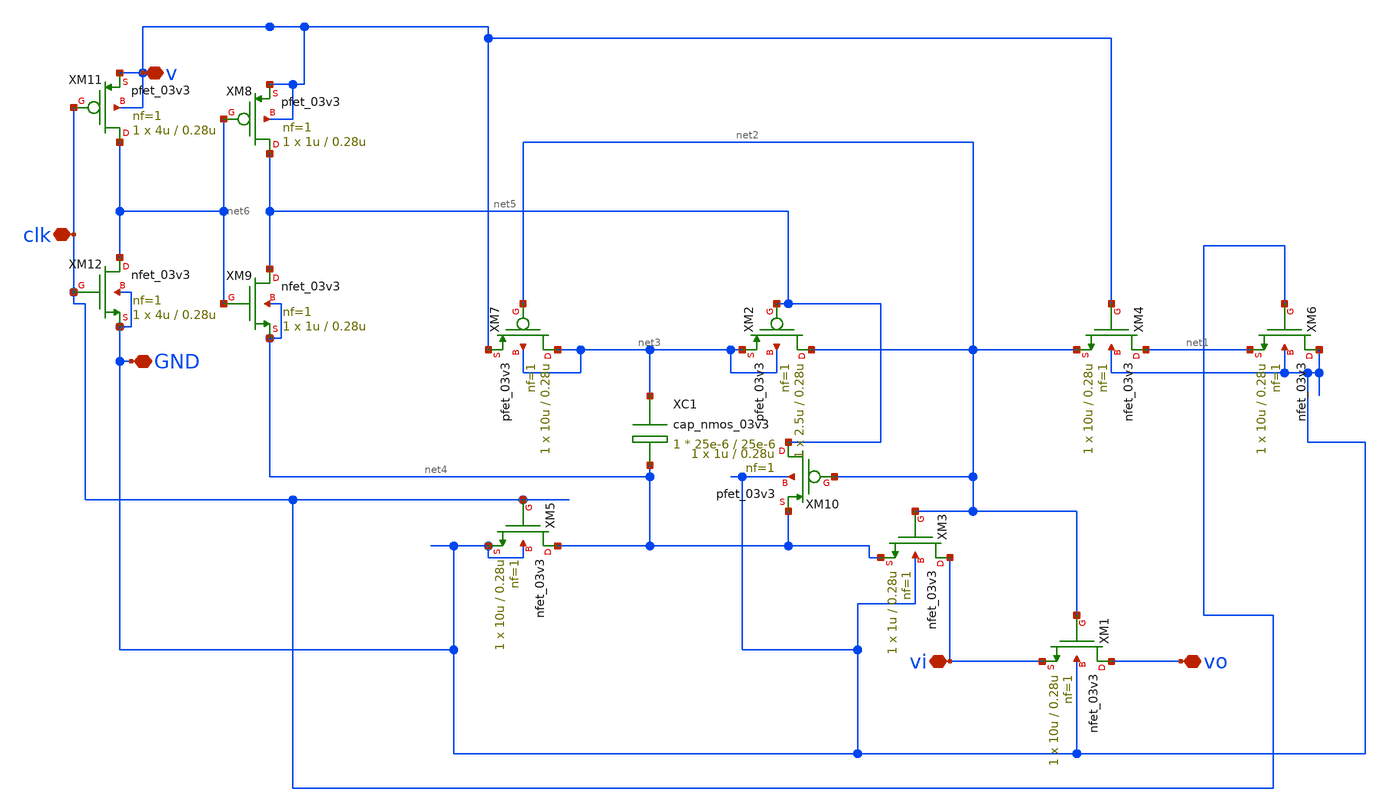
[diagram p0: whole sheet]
** sch_path: Simbolos/btsw.sch
**.subckt btsw vo v GND clk vi
*.iopin vo
*.iopin v
*.iopin GND
*.iopin clk
*.iopin vi
XM1 vo net2 vi GND nfet_03v3 L=0.28u W=10u nf=1 ad='int((nf+1)/2) * W/nf * 0.18u' as='int((nf+2)/2) * W/nf * 0.18u'
+ pd='2*int((nf+1)/2) * (W/nf + 0.18u)' ps='2*int((nf+2)/2) * (W/nf + 0.18u)' nrd='0.18u / W' nrs='0.18u / W'
+ sa=0 sb=0 sd=0 m=1
XM2 net2 net5 net3 net3 pfet_03v3 L=0.28u W=2.5u nf=1 ad='int((nf+1)/2) * W/nf * 0.18u' as='int((nf+2)/2) * W/nf * 0.18u'
+ pd='2*int((nf+1)/2) * (W/nf + 0.18u)' ps='2*int((nf+2)/2) * (W/nf + 0.18u)' nrd='0.18u / W' nrs='0.18u / W'
+ sa=0 sb=0 sd=0 m=1
XM3 vi net2 net4 GND nfet_03v3 L=0.28u W=1u nf=1 ad='int((nf+1)/2) * W/nf * 0.18u' as='int((nf+2)/2) * W/nf * 0.18u'
+ pd='2*int((nf+1)/2) * (W/nf + 0.18u)' ps='2*int((nf+2)/2) * (W/nf + 0.18u)' nrd='0.18u / W' nrs='0.18u / W'
+ sa=0 sb=0 sd=0 m=1
XM4 net1 v net2 GND nfet_03v3 L=0.28u W=10u nf=1 ad='int((nf+1)/2) * W/nf * 0.18u' as='int((nf+2)/2) * W/nf * 0.18u'
+ pd='2*int((nf+1)/2) * (W/nf + 0.18u)' ps='2*int((nf+2)/2) * (W/nf + 0.18u)' nrd='0.18u / W' nrs='0.18u / W'
+ sa=0 sb=0 sd=0 m=1
XM5 net4 clk GND GND nfet_03v3 L=0.28u W=10u nf=1 ad='int((nf+1)/2) * W/nf * 0.18u' as='int((nf+2)/2) * W/nf * 0.18u'
+ pd='2*int((nf+1)/2) * (W/nf + 0.18u)' ps='2*int((nf+2)/2) * (W/nf + 0.18u)' nrd='0.18u / W' nrs='0.18u / W'
+ sa=0 sb=0 sd=0 m=1
XM6 GND clk net1 GND nfet_03v3 L=0.28u W=10u nf=1 ad='int((nf+1)/2) * W/nf * 0.18u' as='int((nf+2)/2) * W/nf * 0.18u'
+ pd='2*int((nf+1)/2) * (W/nf + 0.18u)' ps='2*int((nf+2)/2) * (W/nf + 0.18u)' nrd='0.18u / W' nrs='0.18u / W'
+ sa=0 sb=0 sd=0 m=1
XM7 net3 net2 v net3 pfet_03v3 L=0.28u W=10u nf=1 ad='int((nf+1)/2) * W/nf * 0.18u' as='int((nf+2)/2) * W/nf * 0.18u'
+ pd='2*int((nf+1)/2) * (W/nf + 0.18u)' ps='2*int((nf+2)/2) * (W/nf + 0.18u)' nrd='0.18u / W' nrs='0.18u / W'
+ sa=0 sb=0 sd=0 m=1
XM8 net5 net6 v v pfet_03v3 L=0.28u W=1u nf=1 ad='int((nf+1)/2) * W/nf * 0.18u' as='int((nf+2)/2) * W/nf * 0.18u'
+ pd='2*int((nf+1)/2) * (W/nf + 0.18u)' ps='2*int((nf+2)/2) * (W/nf + 0.18u)' nrd='0.18u / W' nrs='0.18u / W'
+ sa=0 sb=0 sd=0 m=1
XM9 net5 net6 net4 net4 nfet_03v3 L=0.28u W=1u nf=1 ad='int((nf+1)/2) * W/nf * 0.18u' as='int((nf+2)/2) * W/nf * 0.18u'
+ pd='2*int((nf+1)/2) * (W/nf + 0.18u)' ps='2*int((nf+2)/2) * (W/nf + 0.18u)' nrd='0.18u / W' nrs='0.18u / W'
+ sa=0 sb=0 sd=0 m=1
XM10 net5 net2 net4 GND pfet_03v3 L=0.28u W=1u nf=1 ad='int((nf+1)/2) * W/nf * 0.18u' as='int((nf+2)/2) * W/nf * 0.18u'
+ pd='2*int((nf+1)/2) * (W/nf + 0.18u)' ps='2*int((nf+2)/2) * (W/nf + 0.18u)' nrd='0.18u / W' nrs='0.18u / W'
+ sa=0 sb=0 sd=0 m=1
XM11 net6 clk v v pfet_03v3 L=0.28u W=4u nf=1 ad='int((nf+1)/2) * W/nf * 0.18u' as='int((nf+2)/2) * W/nf * 0.18u'
+ pd='2*int((nf+1)/2) * (W/nf + 0.18u)' ps='2*int((nf+2)/2) * (W/nf + 0.18u)' nrd='0.18u / W' nrs='0.18u / W'
+ sa=0 sb=0 sd=0 m=1
XM12 net6 clk GND GND nfet_03v3 L=0.28u W=4u nf=1 ad='int((nf+1)/2) * W/nf * 0.18u' as='int((nf+2)/2) * W/nf * 0.18u'
+ pd='2*int((nf+1)/2) * (W/nf + 0.18u)' ps='2*int((nf+2)/2) * (W/nf + 0.18u)' nrd='0.18u / W' nrs='0.18u / W'
+ sa=0 sb=0 sd=0 m=1
XC1 net3 net4 cap_nmos_03v3 c_width=25e-6 c_length=25e-6 m=1
**** begin user architecture code

.include /foss/pdks/gf180mcuC/libs.tech/ngspice/design.ngspice
.lib /foss/pdks/gf180mcuC/libs.tech/ngspice/sm141064.ngspice typical

**** end user architecture code
**.ends
.end
